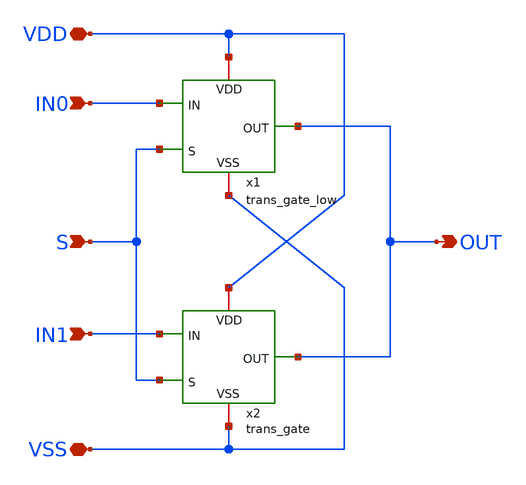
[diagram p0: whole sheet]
** sch_path: SSDOR_1.2V_v2/components/mux2_2/mux2_2.sch
**.subckt mux2_2 IN0 S IN1 VDD VSS OUT
*.ipin IN0
*.ipin S
*.ipin IN1
*.iopin VDD
*.iopin VSS
*.opin OUT
x1 OUT IN0 VDD S VSS trans_gate_low
x2 OUT IN1 VDD S VSS trans_gate
**.ends
.end
